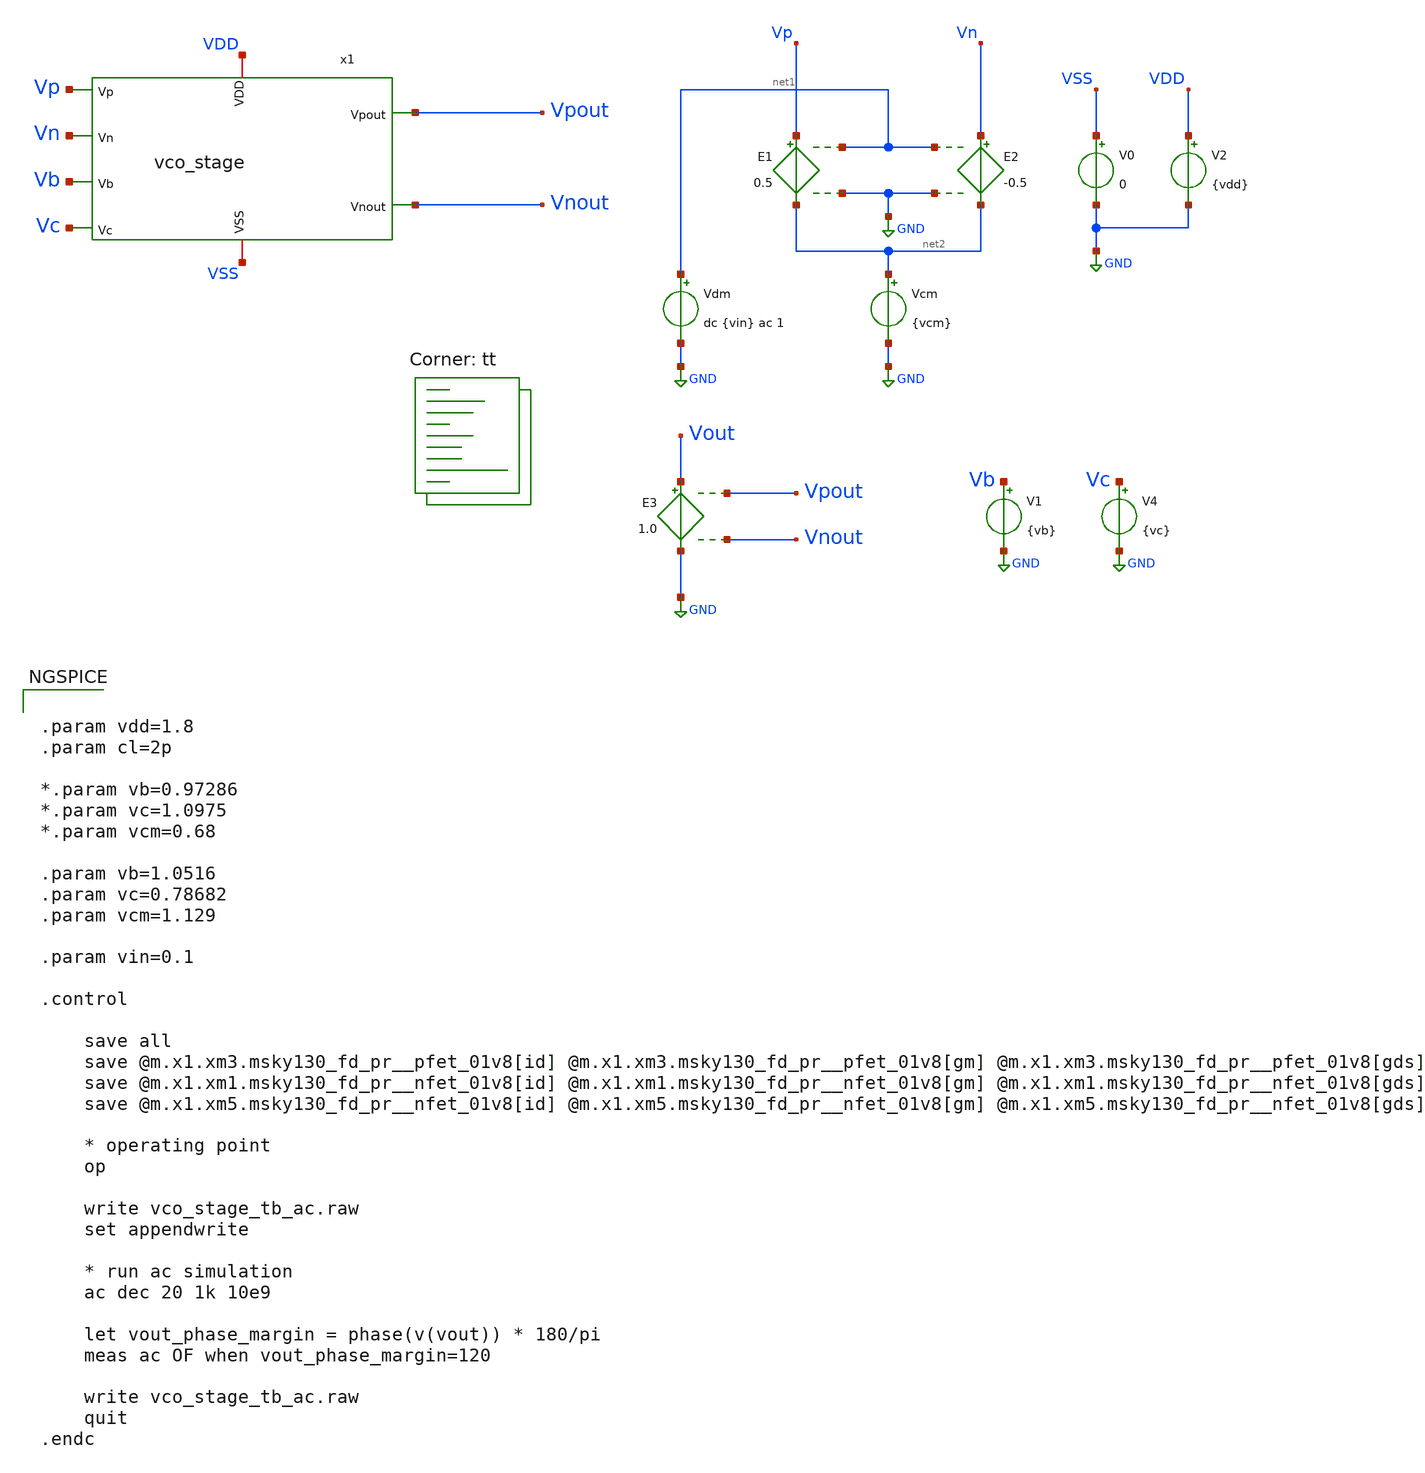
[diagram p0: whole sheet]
** sch_path: xschem/vco_stage_tb_ac.sch
**.subckt vco_stage_tb_ac
V1 Vb GND {vb}
V4 Vc GND {vc}
E1 Vp net2 net1 GND 0.5
E2 Vn net2 net1 GND -0.5
Vdm net1 GND dc {vin} ac 1
Vcm net2 GND {vcm}
V0 VSS GND 0
V2 VDD GND {vdd}
E3 Vout GND Vpout Vnout 1.0
x1 VDD VSS Vp Vn Vb Vc Vpout Vnout vco_stage
**** begin user architecture code
.lib $::SKYWATER_MODELS/sky130.lib.spice tt


.param vdd=1.8
.param cl=2p

*.param vb=0.97286
*.param vc=1.0975
*.param vcm=0.68

.param vb=1.0516
.param vc=0.78682
.param vcm=1.129

.param vin=0.1

.control

    save all
    save @m.x1.xm3.msky130_fd_pr__pfet_01v8[id] @m.x1.xm3.msky130_fd_pr__pfet_01v8[gm]
+ @m.x1.xm3.msky130_fd_pr__pfet_01v8[gds]
    save @m.x1.xm1.msky130_fd_pr__nfet_01v8[id] @m.x1.xm1.msky130_fd_pr__nfet_01v8[gm]
+ @m.x1.xm1.msky130_fd_pr__nfet_01v8[gds]
    save @m.x1.xm5.msky130_fd_pr__nfet_01v8[id] @m.x1.xm5.msky130_fd_pr__nfet_01v8[gm]
+ @m.x1.xm5.msky130_fd_pr__nfet_01v8[gds]

    * operating point
    op

    write vco_stage_tb_ac.raw
    set appendwrite

    * run ac simulation
    ac dec 20 1k 10e9

    let vout_phase_margin = phase(v(vout)) * 180/pi
    meas ac OF when vout_phase_margin=120

    write vco_stage_tb_ac.raw
    quit
.endc


**** end user architecture code
**.ends

* expanding   symbol:  vco_stage.sym # of pins=8
** sym_path: xschem/vco_stage.sym
** sch_path: xschem/vco_stage.sch
.subckt vco_stage VDD VSS Vp Vn Vb Vc Vpout Vnout
*.iopin VDD
*.iopin VSS
*.ipin Vp
*.ipin Vn
*.ipin Vb
*.ipin Vc
*.opin Vpout
*.opin Vnout
XM5 Vds_m5 Vc VSS VSS sky130_fd_pr__nfet_01v8 L={L} W={W} nf=2 ad='int((nf+1)/2) * W/nf * 0.29' as='int((nf+2)/2) * W/nf * 0.29'
+ pd='2*int((nf+1)/2) * (W/nf + 0.29)' ps='2*int((nf+2)/2) * (W/nf + 0.29)' nrd='0.29 / W' nrs='0.29 / W'
+ sa=0 sb=0 sd=0 mult=1 m=1
x1 VDD VSS Vp Vb Vnout Vpout Vds_m5 vco_stage_half
x2 VDD VSS Vn Vb Vpout Vnout Vds_m5 vco_stage_half
.ends


* expanding   symbol:  vco_stage_half.sym # of pins=7
** sym_path: xschem/vco_stage_half.sym
** sch_path: xschem/vco_stage_half.sch
.subckt vco_stage_half VDD VSS Vin Vb Vd Vout Vs
*.iopin VDD
*.iopin VSS
*.ipin Vin
*.ipin Vb
*.ipin Vd
*.opin Vout
*.opin Vs
XM8 VSS Vout VSS VSS sky130_fd_pr__nfet_01v8 L={WLcap} W={WLcap} nf=1 ad='int((nf+1)/2) * W/nf * 0.29'
+ as='int((nf+2)/2) * W/nf * 0.29' pd='2*int((nf+1)/2) * (W/nf + 0.29)' ps='2*int((nf+2)/2) * (W/nf + 0.29)'
+ nrd='0.29 / W' nrs='0.29 / W' sa=0 sb=0 sd=0 mult=1 m=1
XM7 Vout Vd VDD VDD sky130_fd_pr__pfet_01v8 L={L} W={W} nf=2 ad='int((nf+1)/2) * W/nf * 0.29' as='int((nf+2)/2) * W/nf * 0.29'
+ pd='2*int((nf+1)/2) * (W/nf + 0.29)' ps='2*int((nf+2)/2) * (W/nf + 0.29)' nrd='0.29 / W' nrs='0.29 / W'
+ sa=0 sb=0 sd=0 mult=1 m=1
XM3 Vout Vb VDD VDD sky130_fd_pr__pfet_01v8 L={L} W={W} nf=2 ad='int((nf+1)/2) * W/nf * 0.29' as='int((nf+2)/2) * W/nf * 0.29'
+ pd='2*int((nf+1)/2) * (W/nf + 0.29)' ps='2*int((nf+2)/2) * (W/nf + 0.29)' nrd='0.29 / W' nrs='0.29 / W'
+ sa=0 sb=0 sd=0 mult=1 m=1
XM1 Vout Vin Vs VSS sky130_fd_pr__nfet_01v8 L={L} W={W} nf=2 ad='int((nf+1)/2) * W/nf * 0.29' as='int((nf+2)/2) * W/nf * 0.29'
+ pd='2*int((nf+1)/2) * (W/nf + 0.29)' ps='2*int((nf+2)/2) * (W/nf + 0.29)' nrd='0.29 / W' nrs='0.29 / W'
+ sa=0 sb=0 sd=0 mult=1 m=1
.ends

.GLOBAL GND
.end
